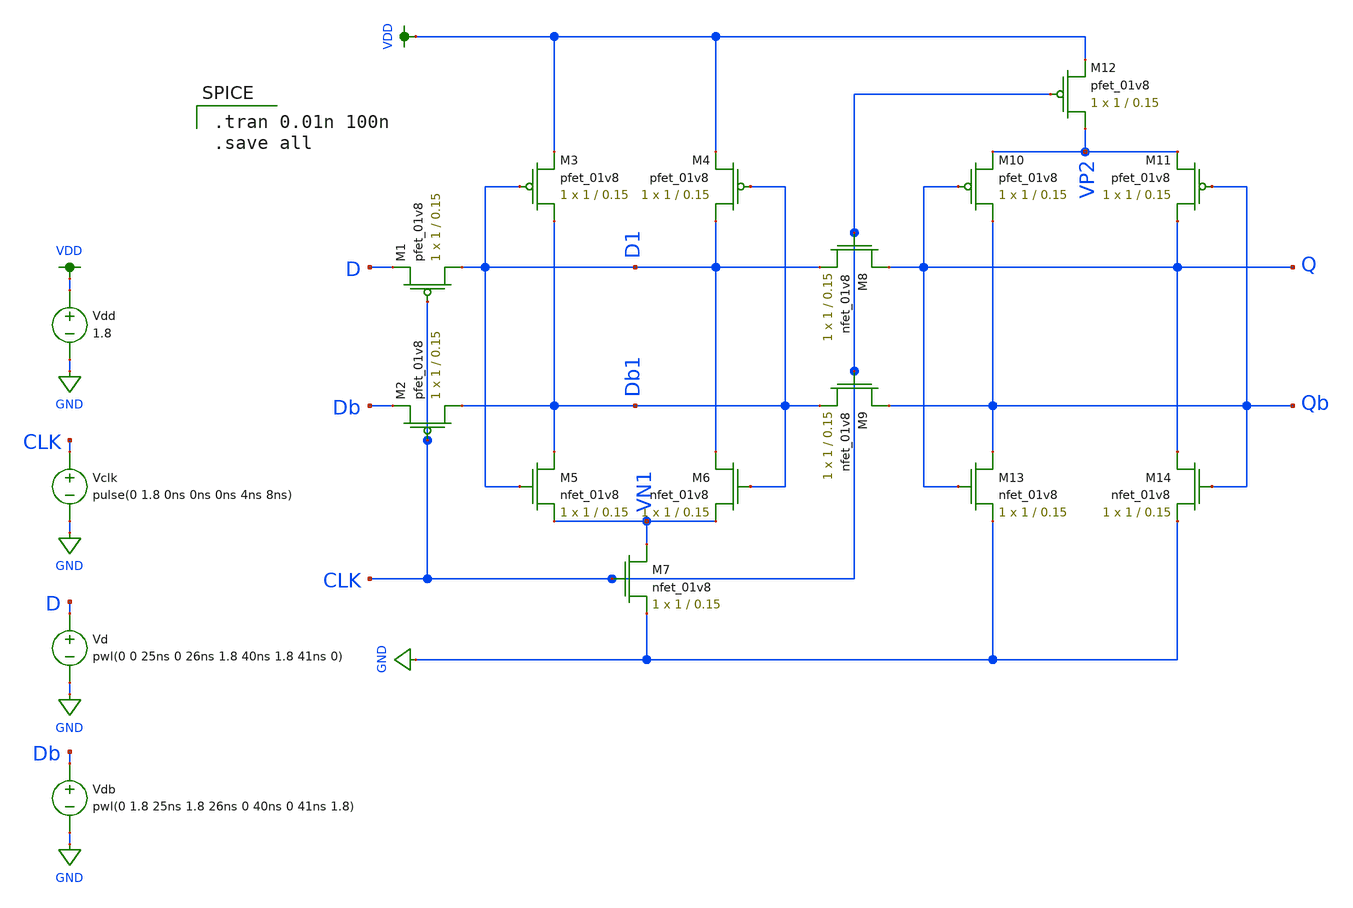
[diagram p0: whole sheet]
** sch_path: simulation/shift_register/andrew_mp2_files/d_flipflop/d_flipflop_test_harness.sch
**.subckt d_flipflop_test_harness
XM1 D1 CLK D VDD sky130_fd_pr__pfet_01v8 L=0.15 W=1 nf=1 ad='int((nf+1)/2) * W/nf * 0.29' as='int((nf+2)/2) * W/nf * 0.29'
+ pd='2*int((nf+1)/2) * (W/nf + 0.29)' ps='2*int((nf+2)/2) * (W/nf + 0.29)' nrd='0.29 / W' nrs='0.29 / W'
+ sa=0 sb=0 sd=0 mult=1 m=1
XM2 Db1 CLK Db VDD sky130_fd_pr__pfet_01v8 L=0.15 W=1 nf=1 ad='int((nf+1)/2) * W/nf * 0.29' as='int((nf+2)/2) * W/nf * 0.29'
+ pd='2*int((nf+1)/2) * (W/nf + 0.29)' ps='2*int((nf+2)/2) * (W/nf + 0.29)' nrd='0.29 / W' nrs='0.29 / W'
+ sa=0 sb=0 sd=0 mult=1 m=1
XM3 Db1 D1 VDD VDD sky130_fd_pr__pfet_01v8 L=0.15 W=1 nf=1 ad='int((nf+1)/2) * W/nf * 0.29' as='int((nf+2)/2) * W/nf * 0.29'
+ pd='2*int((nf+1)/2) * (W/nf + 0.29)' ps='2*int((nf+2)/2) * (W/nf + 0.29)' nrd='0.29 / W' nrs='0.29 / W'
+ sa=0 sb=0 sd=0 mult=1 m=1
XM5 Db1 D1 VN1 GND sky130_fd_pr__nfet_01v8 L=0.15 W=1 nf=1 ad='int((nf+1)/2) * W/nf * 0.29' as='int((nf+2)/2) * W/nf * 0.29'
+ pd='2*int((nf+1)/2) * (W/nf + 0.29)' ps='2*int((nf+2)/2) * (W/nf + 0.29)' nrd='0.29 / W' nrs='0.29 / W'
+ sa=0 sb=0 sd=0 mult=1 m=1
XM7 VN1 CLK GND GND sky130_fd_pr__nfet_01v8 L=0.15 W=1 nf=1 ad='int((nf+1)/2) * W/nf * 0.29' as='int((nf+2)/2) * W/nf * 0.29'
+ pd='2*int((nf+1)/2) * (W/nf + 0.29)' ps='2*int((nf+2)/2) * (W/nf + 0.29)' nrd='0.29 / W' nrs='0.29 / W'
+ sa=0 sb=0 sd=0 mult=1 m=1
XM8 Q CLK D1 GND sky130_fd_pr__nfet_01v8 L=0.15 W=1 nf=1 ad='int((nf+1)/2) * W/nf * 0.29' as='int((nf+2)/2) * W/nf * 0.29'
+ pd='2*int((nf+1)/2) * (W/nf + 0.29)' ps='2*int((nf+2)/2) * (W/nf + 0.29)' nrd='0.29 / W' nrs='0.29 / W'
+ sa=0 sb=0 sd=0 mult=1 m=1
XM9 Qb CLK Db1 GND sky130_fd_pr__nfet_01v8 L=0.15 W=1 nf=1 ad='int((nf+1)/2) * W/nf * 0.29' as='int((nf+2)/2) * W/nf * 0.29'
+ pd='2*int((nf+1)/2) * (W/nf + 0.29)' ps='2*int((nf+2)/2) * (W/nf + 0.29)' nrd='0.29 / W' nrs='0.29 / W'
+ sa=0 sb=0 sd=0 mult=1 m=1
XM10 Qb Q VP2 VDD sky130_fd_pr__pfet_01v8 L=0.15 W=1 nf=1 ad='int((nf+1)/2) * W/nf * 0.29' as='int((nf+2)/2) * W/nf * 0.29'
+ pd='2*int((nf+1)/2) * (W/nf + 0.29)' ps='2*int((nf+2)/2) * (W/nf + 0.29)' nrd='0.29 / W' nrs='0.29 / W'
+ sa=0 sb=0 sd=0 mult=1 m=1
XM11 Q Qb VP2 VDD sky130_fd_pr__pfet_01v8 L=0.15 W=1 nf=1 ad='int((nf+1)/2) * W/nf * 0.29' as='int((nf+2)/2) * W/nf * 0.29'
+ pd='2*int((nf+1)/2) * (W/nf + 0.29)' ps='2*int((nf+2)/2) * (W/nf + 0.29)' nrd='0.29 / W' nrs='0.29 / W'
+ sa=0 sb=0 sd=0 mult=1 m=1
XM12 VP2 CLK VDD VDD sky130_fd_pr__pfet_01v8 L=0.15 W=1 nf=1 ad='int((nf+1)/2) * W/nf * 0.29' as='int((nf+2)/2) * W/nf * 0.29'
+ pd='2*int((nf+1)/2) * (W/nf + 0.29)' ps='2*int((nf+2)/2) * (W/nf + 0.29)' nrd='0.29 / W' nrs='0.29 / W'
+ sa=0 sb=0 sd=0 mult=1 m=1
XM13 Qb Q GND GND sky130_fd_pr__nfet_01v8 L=0.15 W=1 nf=1 ad='int((nf+1)/2) * W/nf * 0.29' as='int((nf+2)/2) * W/nf * 0.29'
+ pd='2*int((nf+1)/2) * (W/nf + 0.29)' ps='2*int((nf+2)/2) * (W/nf + 0.29)' nrd='0.29 / W' nrs='0.29 / W'
+ sa=0 sb=0 sd=0 mult=1 m=1
XM14 Q Qb GND GND sky130_fd_pr__nfet_01v8 L=0.15 W=1 nf=1 ad='int((nf+1)/2) * W/nf * 0.29' as='int((nf+2)/2) * W/nf * 0.29'
+ pd='2*int((nf+1)/2) * (W/nf + 0.29)' ps='2*int((nf+2)/2) * (W/nf + 0.29)' nrd='0.29 / W' nrs='0.29 / W'
+ sa=0 sb=0 sd=0 mult=1 m=1
XM4 D1 Db1 VDD VDD sky130_fd_pr__pfet_01v8 L=0.15 W=1 nf=1 ad='int((nf+1)/2) * W/nf * 0.29' as='int((nf+2)/2) * W/nf * 0.29'
+ pd='2*int((nf+1)/2) * (W/nf + 0.29)' ps='2*int((nf+2)/2) * (W/nf + 0.29)' nrd='0.29 / W' nrs='0.29 / W'
+ sa=0 sb=0 sd=0 mult=1 m=1
XM6 D1 Db1 VN1 GND sky130_fd_pr__nfet_01v8 L=0.15 W=1 nf=1 ad='int((nf+1)/2) * W/nf * 0.29' as='int((nf+2)/2) * W/nf * 0.29'
+ pd='2*int((nf+1)/2) * (W/nf + 0.29)' ps='2*int((nf+2)/2) * (W/nf + 0.29)' nrd='0.29 / W' nrs='0.29 / W'
+ sa=0 sb=0 sd=0 mult=1 m=1
Vdd VDD GND 1.8
Vclk CLK GND pulse(0 1.8 0ns 0ns 0ns 4ns 8ns)
Vd D GND pwl(0 0 25ns 0 26ns 1.8 40ns 1.8 41ns 0)
Vdb Db GND pwl(0 1.8 25ns 1.8 26ns 0 40ns 0 41ns 1.8)
**** begin user architecture code

.option wnflag=1
.lib ~/skywater/skywater-pdk/libraries/sky130_fd_pr_ngspice/latest/models/sky130.lib.spice tt


.tran 0.01n 100n
.save all

**** end user architecture code
**.ends
.GLOBAL VDD
.GLOBAL GND
.end
